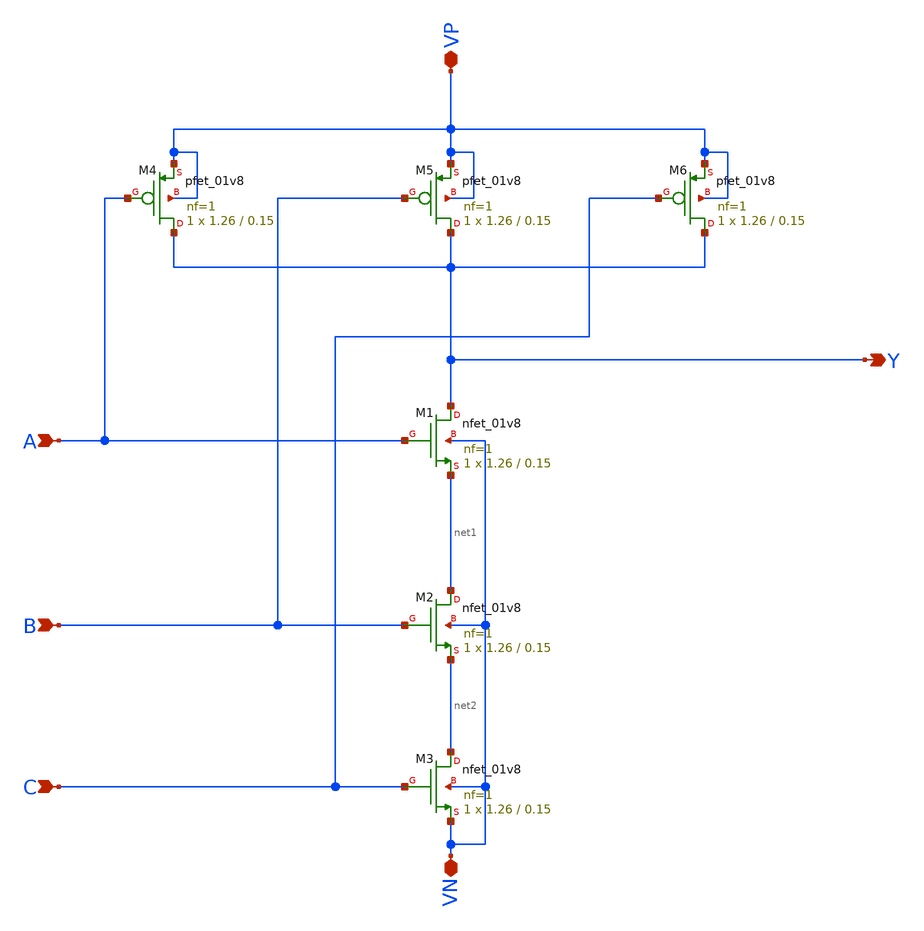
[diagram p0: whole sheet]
** sch_path: component/NAND3/NAND3.sch
**.subckt NAND3 VP VN A B C Y
*.iopin VP
*.iopin VN
*.ipin A
*.ipin B
*.ipin C
*.opin Y
XM1 Y A net1 VN sky130_fd_pr__nfet_01v8 L=0.15 W=1.26 nf=1 ad='int((nf+1)/2) * W/nf * 0.29' as='int((nf+2)/2) * W/nf * 0.29'
+ pd='2*int((nf+1)/2) * (W/nf + 0.29)' ps='2*int((nf+2)/2) * (W/nf + 0.29)' nrd='0.29 / W' nrs='0.29 / W'
+ sa=0 sb=0 sd=0 mult=1 m=1
XM2 net1 B net2 VN sky130_fd_pr__nfet_01v8 L=0.15 W=1.26 nf=1 ad='int((nf+1)/2) * W/nf * 0.29' as='int((nf+2)/2) * W/nf * 0.29'
+ pd='2*int((nf+1)/2) * (W/nf + 0.29)' ps='2*int((nf+2)/2) * (W/nf + 0.29)' nrd='0.29 / W' nrs='0.29 / W'
+ sa=0 sb=0 sd=0 mult=1 m=1
XM3 net2 C VN VN sky130_fd_pr__nfet_01v8 L=0.15 W=1.26 nf=1 ad='int((nf+1)/2) * W/nf * 0.29' as='int((nf+2)/2) * W/nf * 0.29'
+ pd='2*int((nf+1)/2) * (W/nf + 0.29)' ps='2*int((nf+2)/2) * (W/nf + 0.29)' nrd='0.29 / W' nrs='0.29 / W'
+ sa=0 sb=0 sd=0 mult=1 m=1
XM4 Y A VP VP sky130_fd_pr__pfet_01v8 L=0.15 W=1.26 nf=1 ad='int((nf+1)/2) * W/nf * 0.29' as='int((nf+2)/2) * W/nf * 0.29'
+ pd='2*int((nf+1)/2) * (W/nf + 0.29)' ps='2*int((nf+2)/2) * (W/nf + 0.29)' nrd='0.29 / W' nrs='0.29 / W'
+ sa=0 sb=0 sd=0 mult=1 m=1
XM5 Y B VP VP sky130_fd_pr__pfet_01v8 L=0.15 W=1.26 nf=1 ad='int((nf+1)/2) * W/nf * 0.29' as='int((nf+2)/2) * W/nf * 0.29'
+ pd='2*int((nf+1)/2) * (W/nf + 0.29)' ps='2*int((nf+2)/2) * (W/nf + 0.29)' nrd='0.29 / W' nrs='0.29 / W'
+ sa=0 sb=0 sd=0 mult=1 m=1
XM6 Y C VP VP sky130_fd_pr__pfet_01v8 L=0.15 W=1.26 nf=1 ad='int((nf+1)/2) * W/nf * 0.29' as='int((nf+2)/2) * W/nf * 0.29'
+ pd='2*int((nf+1)/2) * (W/nf + 0.29)' ps='2*int((nf+2)/2) * (W/nf + 0.29)' nrd='0.29 / W' nrs='0.29 / W'
+ sa=0 sb=0 sd=0 mult=1 m=1
**.ends
.end
